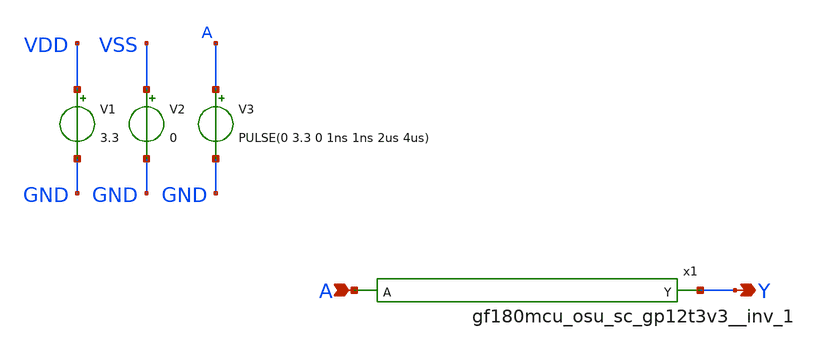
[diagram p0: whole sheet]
** sch_path: examples/digital_tutorial/xschem/sim/tb_inv.sch
**.subckt tb_inv Y A
*.opin Y
*.ipin A
V1 VDD GND 3.3
V2 VSS GND 0
V3 A GND PULSE(0 3.3 0 1ns 1ns 2us 4us)
x1 A Y VDD VSS gf180mcu_osu_sc_gp12t3v3__inv_1
**** begin user architecture code


.include $PDK_ROOT/gf180mcuD/libs.tech/ngspice/design.ngspice
.library "$PDK_ROOT/gf180mcuD/libs.tech/ngspice/sm141064.ngspice" typical

.control
TRAN 0.1u 5u
save all
set filetype=binary
write tb_inv_tran.raw
.endc


**** end user architecture code
**.ends

* expanding   symbol:  gf180mcu_osu_sc_gp12t3v3__inv_1.sym # of pins=2
** sym_path: examples/digital_tutorial/xschem/sim/gf180mcu_osu_sc_gp12t3v3__inv_1.sym
** sch_path: examples/digital_tutorial/xschem/sim/gf180mcu_osu_sc_gp12t3v3__inv_1.sch
.subckt gf180mcu_osu_sc_gp12t3v3__inv_1 A Y VDD VSS
*.ipin A
*.opin Y
XM1 Y A VDD VDD pfet_03v3 L=0.3u W=1.7u nf=1 ad='int((nf+1)/2) * W/nf * 0.18u' as='int((nf+2)/2) * W/nf * 0.18u'
+ pd='2*int((nf+1)/2) * (W/nf + 0.18u)' ps='2*int((nf+2)/2) * (W/nf + 0.18u)' nrd='0.18u / W' nrs='0.18u / W'
+ sa=0 sb=0 sd=0 m=1
XM2 Y A VSS VSS nfet_03v3 L=0.3u W=0.85u nf=1 ad='int((nf+1)/2) * W/nf * 0.18u' as='int((nf+2)/2) * W/nf * 0.18u'
+ pd='2*int((nf+1)/2) * (W/nf + 0.18u)' ps='2*int((nf+2)/2) * (W/nf + 0.18u)' nrd='0.18u / W' nrs='0.18u / W'
+ sa=0 sb=0 sd=0 m=1
.ends

.end
